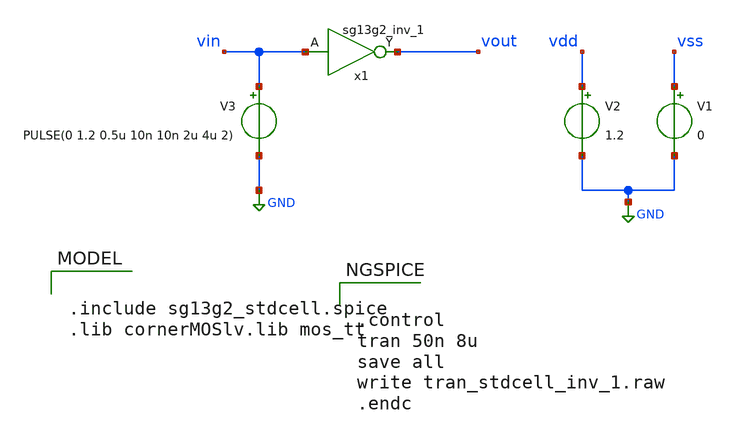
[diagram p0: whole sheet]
** sch_path: ihp-sg13g2/libs.tech/xschem/sg13g2_tests/tran_stdcell_inv_1.sch
**.subckt tran_stdcell_inv_1
x1 vout vin vdd vss sg13g2_inv_1
V1 vss GND 0
V2 vdd GND 1.2
V3 vin GND PULSE(0 1.2 0.5u 10n 10n 2u 4u 2)
**** begin user architecture code

.include sg13g2_stdcell.spice
.lib cornerMOSlv.lib mos_tt



.control
tran 50n 8u
save all
write tran_stdcell_inv_1.raw
.endc


**** end user architecture code
**.ends

* expanding   symbol:  sg13g2_stdcells/sg13g2_inv_1.sym # of pins=2
** sym_path: sg13g2_stdcells/sg13g2_inv_1.sym
** sch_path: sg13g2_stdcells/sg13g2_inv_1.sch
.subckt sg13g2_inv_1 Y A VDD VSS
*.opin Y
*.ipin A
*.iopin VDD
*.iopin VSS
XM1 Y A VSS VSS sg13_lv_nmos w=740.00n l=130.00n ng=1 m=1 mm_ok=1
XM2 Y A VDD VDD sg13_lv_pmos w=1.12u l=130.00n ng=1 m=1 mm_ok=1
.ends

.GLOBAL GND
.end
